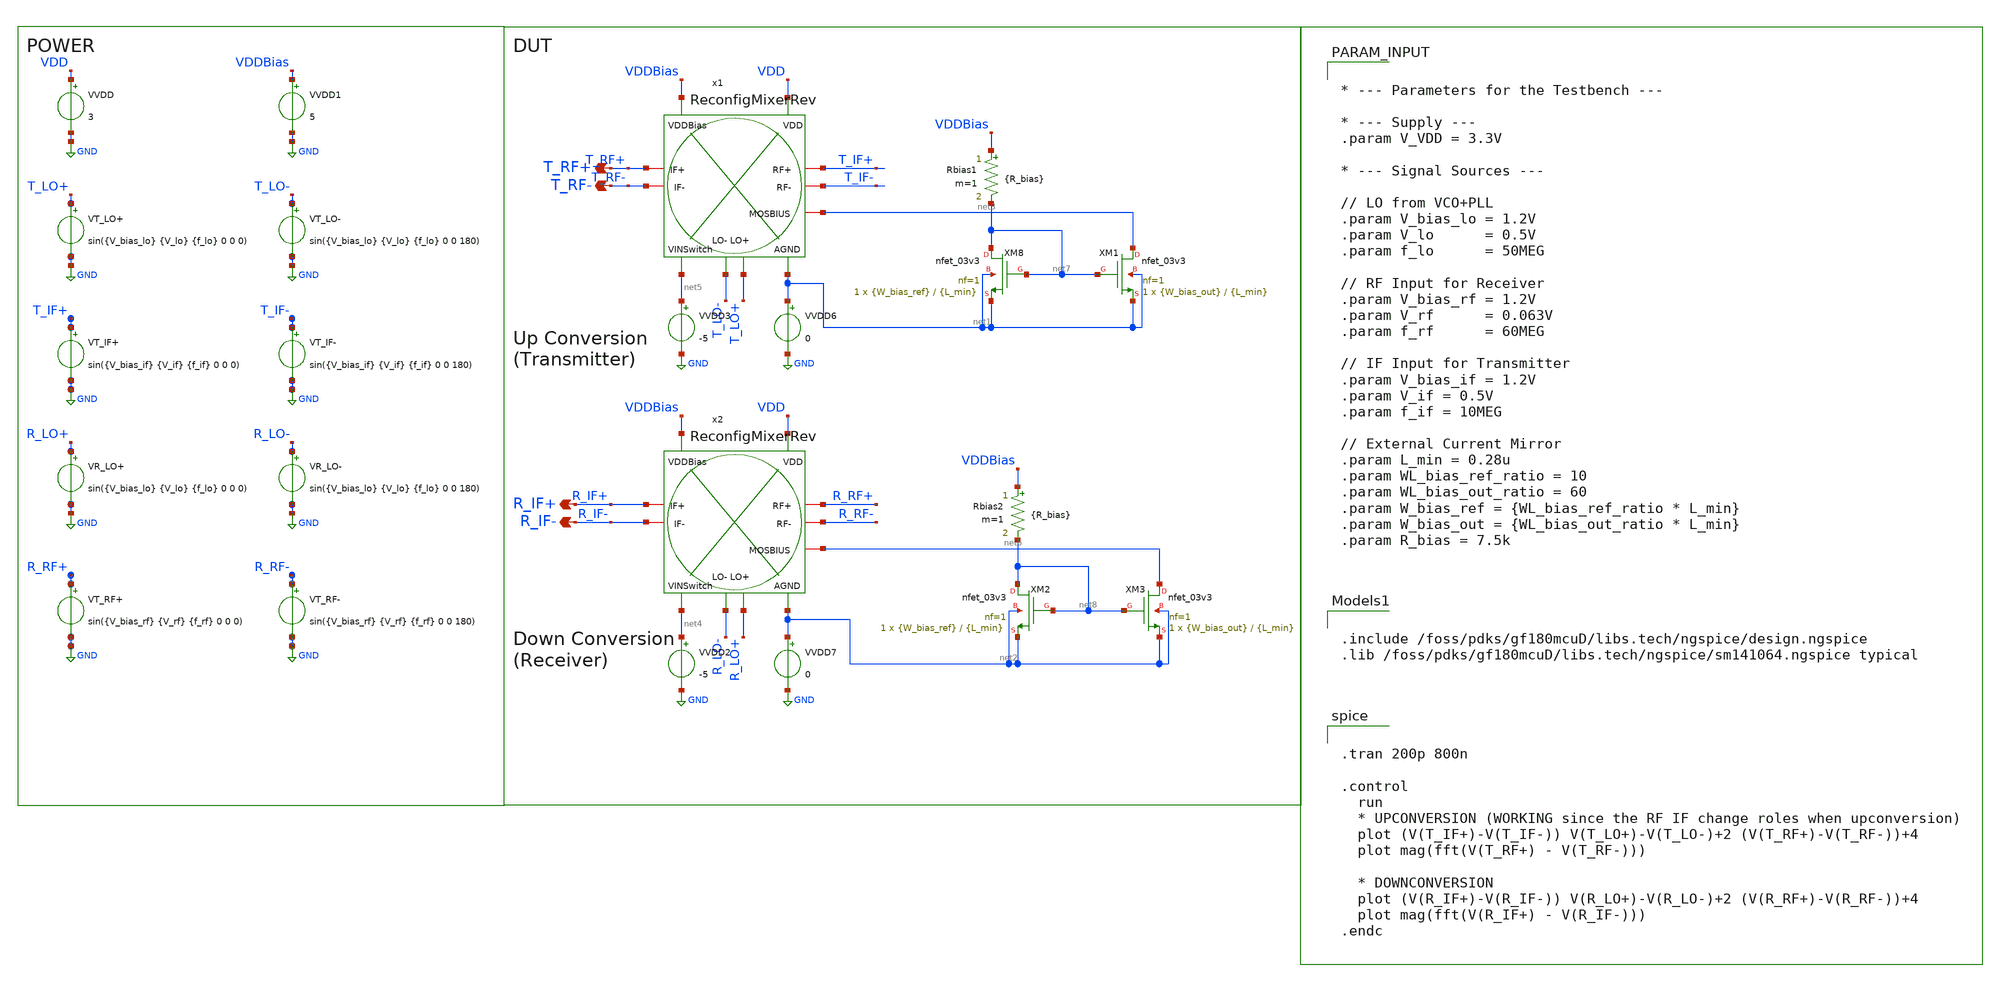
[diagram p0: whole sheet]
** sch_path: Project/1-on-chip/schematic/Mixer/tb_ReconfigMixerExternal.sch
**.subckt tb_ReconfigMixerExternal T_RF+ T_RF- R_IF+ R_IF-
*.opin T_RF+
*.opin T_RF-
*.opin R_IF+
*.opin R_IF-
VVDD VDD GND 3
VT_LO+ T_LO+ GND sin({V_bias_lo} {V_lo} {f_lo} 0 0 0)
VT_LO- T_LO- GND sin({V_bias_lo} {V_lo} {f_lo} 0 0 180)
VT_IF+ T_IF+ GND sin({V_bias_if} {V_if} {f_if} 0 0 0)
VT_IF- T_IF- GND sin({V_bias_if} {V_if} {f_if} 0 0 180)
VR_LO+ R_LO+ GND sin({V_bias_lo} {V_lo} {f_lo} 0 0 0)
VR_LO- R_LO- GND sin({V_bias_lo} {V_lo} {f_lo} 0 0 180)
VT_RF+ R_RF+ GND sin({V_bias_rf} {V_rf} {f_rf} 0 0 0)
VT_RF- R_RF- GND sin({V_bias_rf} {V_rf} {f_rf} 0 0 180)
VVDD1 VDDBias GND 5
x2 VDD R_IF+ R_IF- R_LO+ R_LO- R_RF+ R_RF- net6 VDDBias net2 net4 ReconfigMixerRev
VVDD2 net4 GND -5
VVDD3 net5 GND -5
x1 VDD T_RF+ T_RF- T_LO+ T_LO- T_IF+ T_IF- net3 VDDBias net1 net5 ReconfigMixerRev
VVDD6 net1 GND 0
VVDD7 net2 GND 0
XM8 net7 net7 net1 net1 nfet_03v3 L={L_min} W={W_bias_ref} nf=1 ad='int((nf+1)/2) * W/nf * 0.18u' as='int((nf+2)/2) * W/nf * 0.18u'
+ pd='2*int((nf+1)/2) * (W/nf + 0.18u)' ps='2*int((nf+2)/2) * (W/nf + 0.18u)' nrd='0.18u / W' nrs='0.18u / W'
+ sa=0 sb=0 sd=0 m=1
XM1 net3 net7 net1 net1 nfet_03v3 L={L_min} W={W_bias_out} nf=1 ad='int((nf+1)/2) * W/nf * 0.18u' as='int((nf+2)/2) * W/nf * 0.18u'
+ pd='2*int((nf+1)/2) * (W/nf + 0.18u)' ps='2*int((nf+2)/2) * (W/nf + 0.18u)' nrd='0.18u / W' nrs='0.18u / W'
+ sa=0 sb=0 sd=0 m=1
Rbias1 VDDBias net7 {R_bias} m=1
XM2 net8 net8 net2 net2 nfet_03v3 L={L_min} W={W_bias_ref} nf=1 ad='int((nf+1)/2) * W/nf * 0.18u' as='int((nf+2)/2) * W/nf * 0.18u'
+ pd='2*int((nf+1)/2) * (W/nf + 0.18u)' ps='2*int((nf+2)/2) * (W/nf + 0.18u)' nrd='0.18u / W' nrs='0.18u / W'
+ sa=0 sb=0 sd=0 m=1
XM3 net6 net8 net2 net2 nfet_03v3 L={L_min} W={W_bias_out} nf=1 ad='int((nf+1)/2) * W/nf * 0.18u' as='int((nf+2)/2) * W/nf * 0.18u'
+ pd='2*int((nf+1)/2) * (W/nf + 0.18u)' ps='2*int((nf+2)/2) * (W/nf + 0.18u)' nrd='0.18u / W' nrs='0.18u / W'
+ sa=0 sb=0 sd=0 m=1
Rbias2 VDDBias net8 {R_bias} m=1
**** begin user architecture code

.include /foss/pdks/gf180mcuD/libs.tech/ngspice/design.ngspice
.lib /foss/pdks/gf180mcuD/libs.tech/ngspice/sm141064.ngspice typical



* --- Parameters for the Testbench ---

* --- Supply ---
.param V_VDD = 3.3V

* --- Signal Sources ---

// LO from VCO+PLL
.param V_bias_lo = 1.2V
.param V_lo      = 0.5V
.param f_lo      = 50MEG

// RF Input for Receiver
.param V_bias_rf = 1.2V
.param V_rf      = 0.063V
.param f_rf      = 60MEG

// IF Input for Transmitter
.param V_bias_if = 1.2V
.param V_if = 0.5V
.param f_if = 10MEG

// External Current Mirror
.param L_min = 0.28u
.param WL_bias_ref_ratio = 10
.param WL_bias_out_ratio = 60
.param W_bias_ref = {WL_bias_ref_ratio * L_min}
.param W_bias_out = {WL_bias_out_ratio * L_min}
.param R_bias = 7.5k




.tran 200p 800n

.control
  run
  * UPCONVERSION (WORKING since the RF IF change roles when upconversion)
  plot (V(T_IF+)-V(T_IF-)) V(T_LO+)-V(T_LO-)+2 (V(T_RF+)-V(T_RF-))+4
  plot mag(fft(V(T_RF+) - V(T_RF-)))

  * DOWNCONVERSION
  plot (V(R_IF+)-V(R_IF-)) V(R_LO+)-V(R_LO-)+2 (V(R_RF+)-V(R_RF-))+4
  plot mag(fft(V(R_IF+) - V(R_IF-)))
.endc


**** end user architecture code
**.ends
.GLOBAL GND
.end
